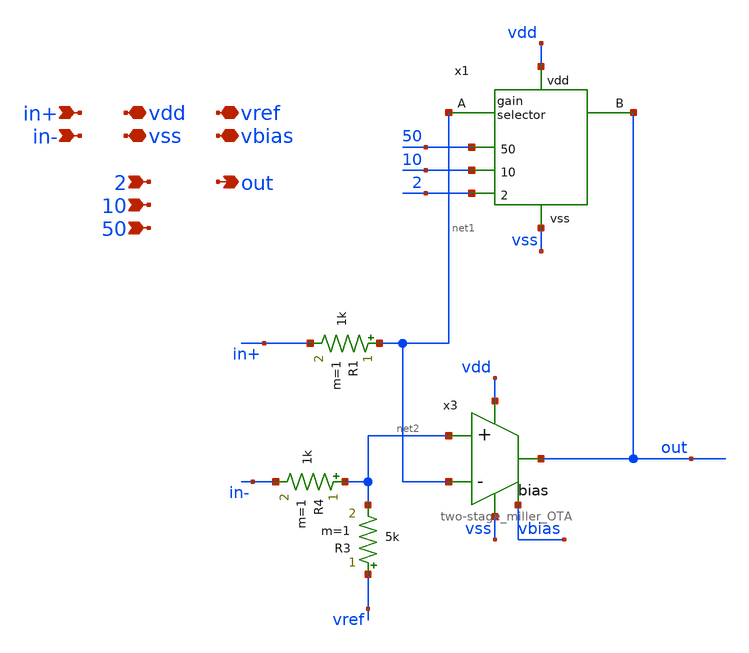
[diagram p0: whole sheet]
** sch_path: design/analog/PGA/PGA.sch
**.subckt PGA out in+ vss in- vdd vref vbias 2 10 50
*.opin out
*.ipin in+
*.iopin vss
*.ipin in-
*.iopin vdd
*.iopin vref
*.iopin vbias
*.ipin 2
*.ipin 10
*.ipin 50
R1 net1 in+ 1k m=1
R3 vref net2 5k m=1
R4 net2 in- 1k m=1
x3 vdd out net2 net1 vbias vss two-stage_miller_OTA
x1 vdd vss 50 net1 10 out 2 gain_selector
**.ends

* expanding   symbol:  acoustic-ranger-dvl-processor/design/analog/OTA/two-stage_miller_OTA.sym # of
*+ pins=6
** sym_path: design/analog/OTA/two-stage_miller_OTA.sym
** sch_path: design/analog/OTA/two-stage_miller_OTA.sch
.subckt two-stage_miller_OTA vdd out in+ in- bias vss
*.ipin in+
*.ipin in-
*.opin out
*.iopin vdd
*.iopin vss
*.ipin bias
XM1 net2 in- net1 vdd pfet_03v3 L=1u W=6.2u nf=1 ad='int((nf+1)/2) * W/nf * 0.18u' as='int((nf+2)/2) * W/nf * 0.18u'
+ pd='2*int((nf+1)/2) * (W/nf + 0.18u)' ps='2*int((nf+2)/2) * (W/nf + 0.18u)' nrd='0.18u / W' nrs='0.18u / W'
+ sa=0 sb=0 sd=0 m=8
XM2 net3 in+ net1 vdd pfet_03v3 L=1u W=6.2u nf=1 ad='int((nf+1)/2) * W/nf * 0.18u' as='int((nf+2)/2) * W/nf * 0.18u'
+ pd='2*int((nf+1)/2) * (W/nf + 0.18u)' ps='2*int((nf+2)/2) * (W/nf + 0.18u)' nrd='0.18u / W' nrs='0.18u / W'
+ sa=0 sb=0 sd=0 m=8
XM14 net3 net2 vss vss nfet_03v3 L=3u W=7.7u nf=4 ad='int((nf+1)/2) * W/nf * 0.18u' as='int((nf+2)/2) * W/nf * 0.18u'
+ pd='2*int((nf+1)/2) * (W/nf + 0.18u)' ps='2*int((nf+2)/2) * (W/nf + 0.18u)' nrd='0.18u / W' nrs='0.18u / W'
+ sa=0 sb=0 sd=0 m=2
XM15 net2 net2 vss vss nfet_03v3 L=3u W=7.7u nf=4 ad='int((nf+1)/2) * W/nf * 0.18u' as='int((nf+2)/2) * W/nf * 0.18u'
+ pd='2*int((nf+1)/2) * (W/nf + 0.18u)' ps='2*int((nf+2)/2) * (W/nf + 0.18u)' nrd='0.18u / W' nrs='0.18u / W'
+ sa=0 sb=0 sd=0 m=2
XM3 out net3 vss vss nfet_03v3 L=3u W=7.7u nf=4 ad='int((nf+1)/2) * W/nf * 0.18u' as='int((nf+2)/2) * W/nf * 0.18u'
+ pd='2*int((nf+1)/2) * (W/nf + 0.18u)' ps='2*int((nf+2)/2) * (W/nf + 0.18u)' nrd='0.18u / W' nrs='0.18u / W'
+ sa=0 sb=0 sd=0 m=12
C1 out net3 5p m=1
XM4 net1 bias vdd vdd pfet_03v3 L=20u W=25.3u nf=2 ad='int((nf+1)/2) * W/nf * 0.18u' as='int((nf+2)/2) * W/nf * 0.18u'
+ pd='2*int((nf+1)/2) * (W/nf + 0.18u)' ps='2*int((nf+2)/2) * (W/nf + 0.18u)' nrd='0.18u / W' nrs='0.18u / W'
+ sa=0 sb=0 sd=0 m=2
XM5 out bias vdd vdd pfet_03v3 L=20u W=25.3u nf=2 ad='int((nf+1)/2) * W/nf * 0.18u' as='int((nf+2)/2) * W/nf * 0.18u'
+ pd='2*int((nf+1)/2) * (W/nf + 0.18u)' ps='2*int((nf+2)/2) * (W/nf + 0.18u)' nrd='0.18u / W' nrs='0.18u / W'
+ sa=0 sb=0 sd=0 m=6
.ends


* expanding   symbol:  acoustic-ranger-dvl-processor/design/analog/PGA/gain_selector.sym # of pins=7
** sym_path: design/analog/PGA/gain_selector.sym
** sch_path: design/analog/PGA/gain_selector.sch
.subckt gain_selector vdd vss 50 A 10 B 2
*.iopin A
*.iopin B
*.ipin 2
*.ipin 10
*.ipin 50
*.iopin vdd
*.iopin vss
x9 A 2b 2 vdd vss net1 Transmission_Gate
R5 net1 B 2k m=1
x10 A 10b 10 vdd vss net2 Transmission_Gate
R6 net2 B 10k m=1
x11 A 50b 50 vdd vss net3 Transmission_Gate
R7 net3 B 50k m=1
XM9 50b 50 vdd vdd pfet_03v3 L=0.28u W=2u nf=1 ad='int((nf+1)/2) * W/nf * 0.18u' as='int((nf+2)/2) * W/nf * 0.18u'
+ pd='2*int((nf+1)/2) * (W/nf + 0.18u)' ps='2*int((nf+2)/2) * (W/nf + 0.18u)' nrd='0.18u / W' nrs='0.18u / W'
+ sa=0 sb=0 sd=0 m=1
XM10 50b 50 vss vss nfet_03v3 L=0.28u W=1u nf=1 ad='int((nf+1)/2) * W/nf * 0.18u' as='int((nf+2)/2) * W/nf * 0.18u'
+ pd='2*int((nf+1)/2) * (W/nf + 0.18u)' ps='2*int((nf+2)/2) * (W/nf + 0.18u)' nrd='0.18u / W' nrs='0.18u / W'
+ sa=0 sb=0 sd=0 m=1
XM11 10b 10 vdd vdd pfet_03v3 L=0.28u W=2u nf=1 ad='int((nf+1)/2) * W/nf * 0.18u' as='int((nf+2)/2) * W/nf * 0.18u'
+ pd='2*int((nf+1)/2) * (W/nf + 0.18u)' ps='2*int((nf+2)/2) * (W/nf + 0.18u)' nrd='0.18u / W' nrs='0.18u / W'
+ sa=0 sb=0 sd=0 m=1
XM12 10b 10 vss vss nfet_03v3 L=0.28u W=1u nf=1 ad='int((nf+1)/2) * W/nf * 0.18u' as='int((nf+2)/2) * W/nf * 0.18u'
+ pd='2*int((nf+1)/2) * (W/nf + 0.18u)' ps='2*int((nf+2)/2) * (W/nf + 0.18u)' nrd='0.18u / W' nrs='0.18u / W'
+ sa=0 sb=0 sd=0 m=1
XM13 2b 2 vdd vdd pfet_03v3 L=0.28u W=2u nf=1 ad='int((nf+1)/2) * W/nf * 0.18u' as='int((nf+2)/2) * W/nf * 0.18u'
+ pd='2*int((nf+1)/2) * (W/nf + 0.18u)' ps='2*int((nf+2)/2) * (W/nf + 0.18u)' nrd='0.18u / W' nrs='0.18u / W'
+ sa=0 sb=0 sd=0 m=1
XM14 2b 2 vss vss nfet_03v3 L=0.28u W=1u nf=1 ad='int((nf+1)/2) * W/nf * 0.18u' as='int((nf+2)/2) * W/nf * 0.18u'
+ pd='2*int((nf+1)/2) * (W/nf + 0.18u)' ps='2*int((nf+2)/2) * (W/nf + 0.18u)' nrd='0.18u / W' nrs='0.18u / W'
+ sa=0 sb=0 sd=0 m=1
.ends


* expanding   symbol:  Transmission_Gate.sym # of pins=6
** sym_path: design/analog/transmission_gate/Transmission_Gate.sym
** sch_path: design/analog/transmission_gate/Transmission_Gate.sch
.subckt Transmission_Gate A en_b en vdd vss B
*.ipin en_b
*.iopin A
*.iopin B
*.ipin en
*.iopin vdd
*.iopin vss
XM1 B en_b A vdd pfet_03v3 L=0.28u W=20u nf=10 ad='int((nf+1)/2) * W/nf * 0.18u' as='int((nf+2)/2) * W/nf * 0.18u'
+ pd='2*int((nf+1)/2) * (W/nf + 0.18u)' ps='2*int((nf+2)/2) * (W/nf + 0.18u)' nrd='0.18u / W' nrs='0.18u / W'
+ sa=0 sb=0 sd=0 m=8
XM2 A en B vss nfet_03v3 L=0.28u W=10u nf=5 ad='int((nf+1)/2) * W/nf * 0.18u' as='int((nf+2)/2) * W/nf * 0.18u'
+ pd='2*int((nf+1)/2) * (W/nf + 0.18u)' ps='2*int((nf+2)/2) * (W/nf + 0.18u)' nrd='0.18u / W' nrs='0.18u / W'
+ sa=0 sb=0 sd=0 m=8
.ends

.end
